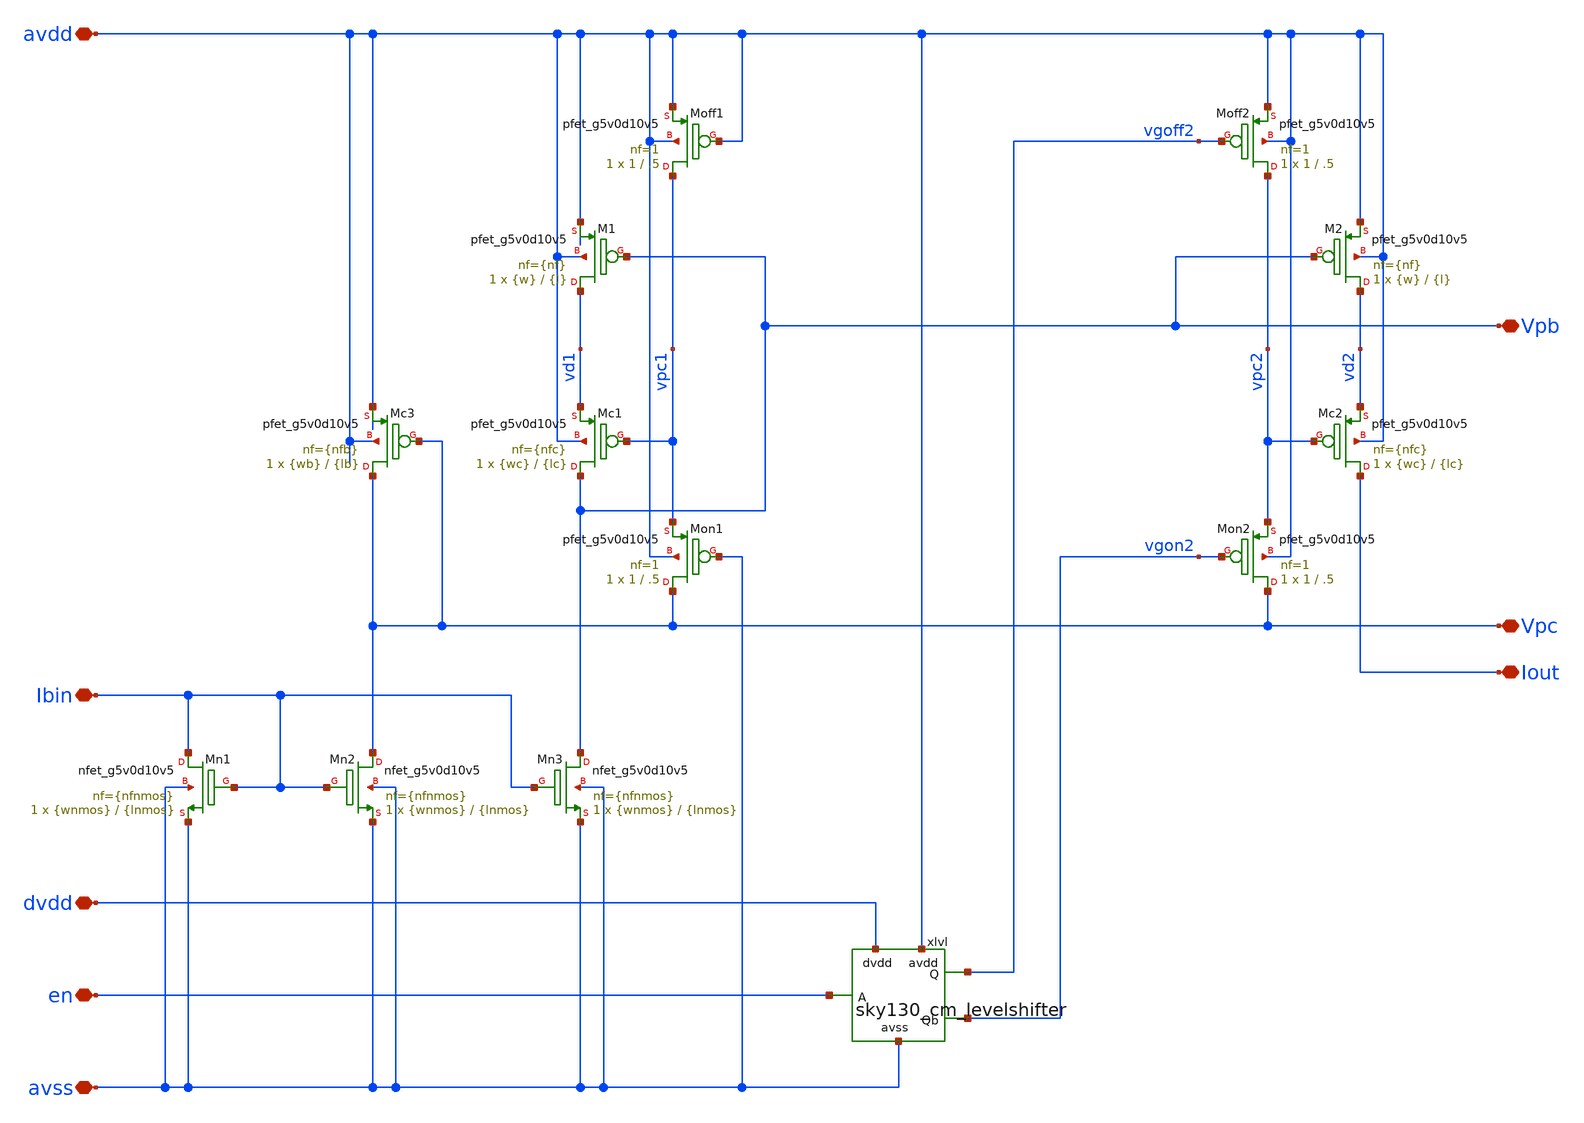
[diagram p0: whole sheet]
** sch_path: xschem/sky130_cm_ip__biasgen.sch
**.subckt sky130_cm_ip__biasgen avss avdd Ibin Vpb Vpc Iout dvdd en
*.iopin avss
*.iopin avdd
*.iopin Ibin
*.iopin Vpb
*.iopin Vpc
*.iopin Iout
*.iopin dvdd
*.iopin en
XMc1 Vpb vpc1 vd1 avdd sky130_fd_pr__pfet_g5v0d10v5 L={lc} W={wc} nf={nfc} ad='int(({nfc} + 1)/2) * {wc} / {nfc} * 0.29'
+ as='int(({nfc} + 2)/2) * {wc} / {nfc} * 0.29' pd='2*int(({nfc} + 1)/2) * ({wc} / {nfc} + 0.29)' ps='2*int(({nfc} + 2)/2) * ({wc} / {nfc} + 0.29)'
+ nrd='0.29 / {wc} ' nrs='0.29 / {wc} ' sa=0 sb=0 sd=0 mult=1 m=1
XM1 vd1 Vpb avdd avdd sky130_fd_pr__pfet_g5v0d10v5 L={l} W={w} nf={nf} ad='int(({nf} + 1)/2) * {w} / {nf} * 0.29'
+ as='int(({nf} + 2)/2) * {w} / {nf} * 0.29' pd='2*int(({nf} + 1)/2) * ({w} / {nf} + 0.29)' ps='2*int(({nf} + 2)/2) * ({w} / {nf} + 0.29)'
+ nrd='0.29 / {w} ' nrs='0.29 / {w} ' sa=0 sb=0 sd=0 mult=1 m=1
XMc2 Iout vpc2 vd2 avdd sky130_fd_pr__pfet_g5v0d10v5 L={lc} W={wc} nf={nfc} ad='int(({nfc} + 1)/2) * {wc} / {nfc} * 0.29'
+ as='int(({nfc} + 2)/2) * {wc} / {nfc} * 0.29' pd='2*int(({nfc} + 1)/2) * ({wc} / {nfc} + 0.29)' ps='2*int(({nfc} + 2)/2) * ({wc} / {nfc} + 0.29)'
+ nrd='0.29 / {wc} ' nrs='0.29 / {wc} ' sa=0 sb=0 sd=0 mult=1 m=1
XM2 vd2 Vpb avdd avdd sky130_fd_pr__pfet_g5v0d10v5 L={l} W={w} nf={nf} ad='int(({nf} + 1)/2) * {w} / {nf} * 0.29'
+ as='int(({nf} + 2)/2) * {w} / {nf} * 0.29' pd='2*int(({nf} + 1)/2) * ({w} / {nf} + 0.29)' ps='2*int(({nf} + 2)/2) * ({w} / {nf} + 0.29)'
+ nrd='0.29 / {w} ' nrs='0.29 / {w} ' sa=0 sb=0 sd=0 mult=1 m=1
XMc3 Vpc Vpc avdd avdd sky130_fd_pr__pfet_g5v0d10v5 L={lb} W={wb} nf={nfb} ad='int(({nfb} + 1)/2) * {wb} / {nfb} * 0.29'
+ as='int(({nfb} + 2)/2) * {wb} / {nfb} * 0.29' pd='2*int(({nfb} + 1)/2) * ({wb} / {nfb} + 0.29)' ps='2*int(({nfb} + 2)/2) * ({wb} / {nfb} + 0.29)'
+ nrd='0.29 / {wb} ' nrs='0.29 / {wb} ' sa=0 sb=0 sd=0 mult=1 m=1
XMn1 Ibin Ibin avss avss sky130_fd_pr__nfet_g5v0d10v5 L={lnmos} W={wnmos} nf={nfnmos} ad='int(({nfnmos} + 1)/2) * {wnmos} / {nfnmos} * 0.29'
+ as='int(({nfnmos} + 2)/2) * {wnmos} / {nfnmos} * 0.29' pd='2*int(({nfnmos} + 1)/2) * ({wnmos} / {nfnmos} + 0.29)'
+ ps='2*int(({nfnmos} + 2)/2) * ({wnmos} / {nfnmos} + 0.29)' nrd='0.29 / {wnmos} ' nrs='0.29 / {wnmos} '
+ sa=0 sb=0 sd=0 mult=1 m=1
XMn2 Vpc Ibin avss avss sky130_fd_pr__nfet_g5v0d10v5 L={lnmos} W={wnmos} nf={nfnmos} ad='int(({nfnmos} + 1)/2) * {wnmos} / {nfnmos} * 0.29'
+ as='int(({nfnmos} + 2)/2) * {wnmos} / {nfnmos} * 0.29' pd='2*int(({nfnmos} + 1)/2) * ({wnmos} / {nfnmos} + 0.29)'
+ ps='2*int(({nfnmos} + 2)/2) * ({wnmos} / {nfnmos} + 0.29)' nrd='0.29 / {wnmos} ' nrs='0.29 / {wnmos} '
+ sa=0 sb=0 sd=0 mult=1 m=1
XMn3 Vpb Ibin avss avss sky130_fd_pr__nfet_g5v0d10v5 L={lnmos} W={wnmos} nf={nfnmos} ad='int(({nfnmos} + 1)/2) * {wnmos} / {nfnmos} * 0.29'
+ as='int(({nfnmos} + 2)/2) * {wnmos} / {nfnmos} * 0.29' pd='2*int(({nfnmos} + 1)/2) * ({wnmos} / {nfnmos} + 0.29)'
+ ps='2*int(({nfnmos} + 2)/2) * ({wnmos} / {nfnmos} + 0.29)' nrd='0.29 / {wnmos} ' nrs='0.29 / {wnmos} '
+ sa=0 sb=0 sd=0 mult=1 m=1
XMon1 Vpc avss vpc1 avdd sky130_fd_pr__pfet_g5v0d10v5 L=.5 W=1 nf=1 ad='int((1 + 1)/2) * 1 / 1 * 0.29'
+ as='int((1 + 2)/2) * 1 / 1 * 0.29' pd='2*int((1 + 1)/2) * (1 / 1 + 0.29)' ps='2*int((1 + 2)/2) * (1 / 1 + 0.29)'
+ nrd='0.29 / 1 ' nrs='0.29 / 1 ' sa=0 sb=0 sd=0 mult=1 m=1
XMoff1 vpc1 avdd avdd avdd sky130_fd_pr__pfet_g5v0d10v5 L=.5 W=1 nf=1 ad='int((1 + 1)/2) * 1 / 1 * 0.29'
+ as='int((1 + 2)/2) * 1 / 1 * 0.29' pd='2*int((1 + 1)/2) * (1 / 1 + 0.29)' ps='2*int((1 + 2)/2) * (1 / 1 + 0.29)'
+ nrd='0.29 / 1 ' nrs='0.29 / 1 ' sa=0 sb=0 sd=0 mult=1 m=1
XMon2 Vpc vgon2 vpc2 avdd sky130_fd_pr__pfet_g5v0d10v5 L=.5 W=1 nf=1 ad='int((1 + 1)/2) * 1 / 1 * 0.29'
+ as='int((1 + 2)/2) * 1 / 1 * 0.29' pd='2*int((1 + 1)/2) * (1 / 1 + 0.29)' ps='2*int((1 + 2)/2) * (1 / 1 + 0.29)'
+ nrd='0.29 / 1 ' nrs='0.29 / 1 ' sa=0 sb=0 sd=0 mult=1 m=1
XMoff2 vpc2 vgoff2 avdd avdd sky130_fd_pr__pfet_g5v0d10v5 L=.5 W=1 nf=1 ad='int((1 + 1)/2) * 1 / 1 * 0.29'
+ as='int((1 + 2)/2) * 1 / 1 * 0.29' pd='2*int((1 + 1)/2) * (1 / 1 + 0.29)' ps='2*int((1 + 2)/2) * (1 / 1 + 0.29)'
+ nrd='0.29 / 1 ' nrs='0.29 / 1 ' sa=0 sb=0 sd=0 mult=1 m=1
xlvl avdd vgoff2 dvdd vgon2 en avss sky130_cm_levelshifter
**.ends

* expanding   symbol:  xschem/sky130_cm_levelshifter.sym # of pins=6
** sym_path: xschem/sky130_cm_levelshifter.sym
** sch_path: xschem/sky130_cm_levelshifter.sch
.subckt sky130_cm_levelshifter avdd Q dvdd Qb A avss
*.iopin avss
*.iopin avdd
*.iopin A
*.iopin dvdd
*.iopin Qb
*.iopin Q
XMnl1 Q ab avss avss sky130_fd_pr__nfet_g5v0d10v5 L=0.5 W=6 nf=1 ad='int((1 + 1)/2) * 6 / 1 * 0.29' as='int((1 + 2)/2) * 6 / 1 * 0.29'
+ pd='2*int((1 + 1)/2) * (6 / 1 + 0.29)' ps='2*int((1 + 2)/2) * (6 / 1 + 0.29)' nrd='0.29 / 6 ' nrs='0.29 / 6 '
+ sa=0 sb=0 sd=0 mult=1 m=1
XMnl2 Qb abb avss avss sky130_fd_pr__nfet_g5v0d10v5 L=0.5 W=6 nf=1 ad='int((1 + 1)/2) * 6 / 1 * 0.29'
+ as='int((1 + 2)/2) * 6 / 1 * 0.29' pd='2*int((1 + 1)/2) * (6 / 1 + 0.29)' ps='2*int((1 + 2)/2) * (6 / 1 + 0.29)'
+ nrd='0.29 / 6 ' nrs='0.29 / 6 ' sa=0 sb=0 sd=0 mult=1 m=1
XMpl1 Q Qb avdd avdd sky130_fd_pr__pfet_g5v0d10v5 L=0.5 W=2 nf=1 ad='int((1 + 1)/2) * 2 / 1 * 0.29' as='int((1 + 2)/2) * 2 / 1 * 0.29'
+ pd='2*int((1 + 1)/2) * (2 / 1 + 0.29)' ps='2*int((1 + 2)/2) * (2 / 1 + 0.29)' nrd='0.29 / 2 ' nrs='0.29 / 2 '
+ sa=0 sb=0 sd=0 mult=1 m=1
XMpl2 Qb Q avdd avdd sky130_fd_pr__pfet_g5v0d10v5 L=0.5 W=2 nf=1 ad='int((1 + 1)/2) * 2 / 1 * 0.29' as='int((1 + 2)/2) * 2 / 1 * 0.29'
+ pd='2*int((1 + 1)/2) * (2 / 1 + 0.29)' ps='2*int((1 + 2)/2) * (2 / 1 + 0.29)' nrd='0.29 / 2 ' nrs='0.29 / 2 '
+ sa=0 sb=0 sd=0 mult=1 m=1
XMn1 ab A avss avss sky130_fd_pr__nfet_01v8 L=0.15 W=1 nf=1 ad='int((1 + 1)/2) * 1 / 1 * 0.29' as='int((1 + 2)/2) * 1 / 1 * 0.29'
+ pd='2*int((1 + 1)/2) * (1 / 1 + 0.29)' ps='2*int((1 + 2)/2) * (1 / 1 + 0.29)' nrd='0.29 / 1 ' nrs='0.29 / 1 '
+ sa=0 sb=0 sd=0 mult=1 m=1
XMp1 ab A dvdd dvdd sky130_fd_pr__pfet_01v8 L=0.15 W=2 nf=1 ad='int((nf+1)/2) * W/nf * 0.29' as='int((nf+2)/2) * W/nf * 0.29'
+ pd='2*int((nf+1)/2) * (W/nf + 0.29)' ps='2*int((nf+2)/2) * (W/nf + 0.29)' nrd='0.29 / W' nrs='0.29 / W'
+ sa=0 sb=0 sd=0 mult=1 m=1
XMn2 abb ab avss avss sky130_fd_pr__nfet_01v8 L=0.15 W=1 nf=1 ad='int((1 + 1)/2) * 1 / 1 * 0.29' as='int((1 + 2)/2) * 1 / 1 * 0.29'
+ pd='2*int((1 + 1)/2) * (1 / 1 + 0.29)' ps='2*int((1 + 2)/2) * (1 / 1 + 0.29)' nrd='0.29 / 1 ' nrs='0.29 / 1 '
+ sa=0 sb=0 sd=0 mult=1 m=1
XMp2 abb ab dvdd dvdd sky130_fd_pr__pfet_01v8 L=0.15 W=2 nf=1 ad='int((nf+1)/2) * W/nf * 0.29' as='int((nf+2)/2) * W/nf * 0.29'
+ pd='2*int((nf+1)/2) * (W/nf + 0.29)' ps='2*int((nf+2)/2) * (W/nf + 0.29)' nrd='0.29 / W' nrs='0.29 / W'
+ sa=0 sb=0 sd=0 mult=1 m=1
.ends

.end
